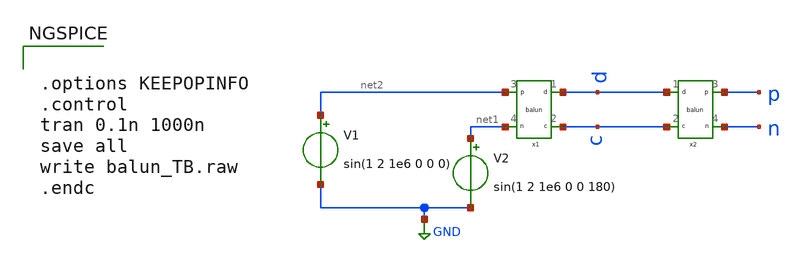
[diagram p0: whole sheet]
** sch_path: examples/xschem/balun_TB.sch
**.subckt balun_TB
V1 net2 GND sin(1 2 1e6 0 0 0)
V2 net1 GND sin(1 2 1e6 0 0 180)
x2 d c p n balun
x1 d c net2 net1 balun
**** begin user architecture code


.options KEEPOPINFO
.control
tran 0.1n 1000n
save all
write balun_TB.raw
.endc


**** end user architecture code
**.ends

* expanding   symbol:  balun.sym # of pins=4
** sym_path: examples/xschem/balun.sym
** sch_path: examples/xschem/balun.sch
.subckt balun 1 2 3 4
*.iopin 1
*.iopin 2
*.iopin 3
*.iopin 4
E1 5 2 1 0 0.5
V1 3 5 0
F1 1 0 V1 -0.5
R1 1 0 1T m=1
E2 6 4 1 0 0.5
V2 2 7 0
F2 1 0 V2 -0.5
R2 7 6 1u m=1
.ends

.GLOBAL GND
.end
